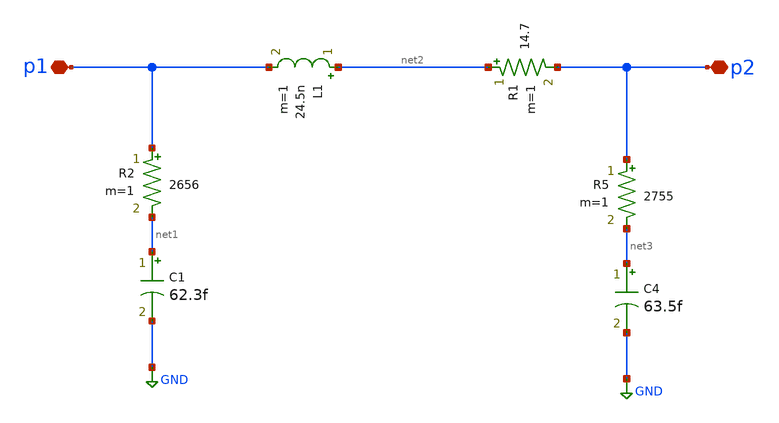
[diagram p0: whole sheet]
** sch_path: LNA7096-main/schematic/xschem/01_lna/ld.sch
**.subckt ld p1 p2
*.iopin p1
*.iopin p2
L1 net2 p1 24.5n m=1
R1 net2 p2 14.7 m=1
R2 p1 net1 2656 m=1
C1 net1 GND 62.3f m=1
R5 p2 net3 2755 m=1
C4 net3 GND 63.5f m=1
**.ends
.GLOBAL GND
.end
